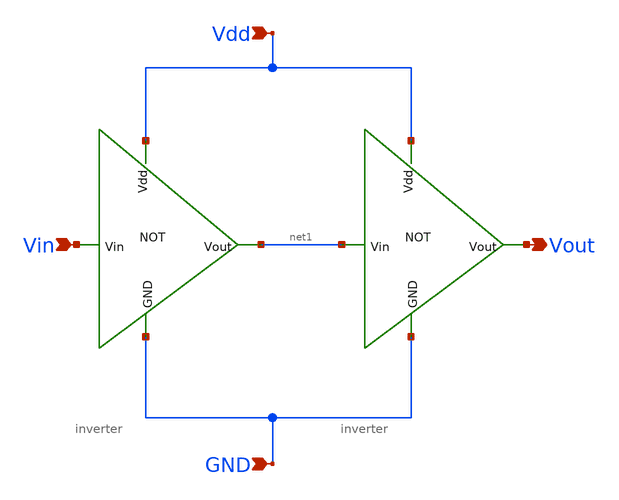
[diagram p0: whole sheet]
** sch_path: buffer.sch
**.subckt buffer Vin GND Vdd Vout
*.ipin Vin
*.ipin GND
*.ipin Vdd
*.opin Vout
x1 Vdd Vin net1 GND inverter
x2 Vdd net1 Vout GND inverter
**.ends

* expanding   symbol:  /home/jetha/Projects/sky130/SAR_ADC/inverter/inverter.sym # of pins=4
** sym_path: inverter.sym
** sch_path: inverter.sch
.subckt inverter Vdd Vin Vout GND
*.ipin Vin
*.ipin Vdd
*.ipin GND
*.opin Vout
XM2 Vout Vin GND GND sky130_fd_pr__nfet_01v8 L=0.15 W=1 nf=1 ad='int((1 + 1)/2) * 1 / 1 * 0.29' as='int((1 + 2)/2) * 1 / 1 * 0.29'
+ pd='2*int((1 + 1)/2) * (1 / 1 + 0.29)' ps='2*int((1 + 2)/2) * (1 / 1 + 0.29)' nrd='0.29 / 1 ' nrs='0.29 / 1 '
+ sa=0 sb=0 sd=0 mult=1 m=1
XM1 Vout Vin Vdd Vdd sky130_fd_pr__pfet_01v8 L=0.15 W=2 nf=1 ad='int((1 + 1)/2) * 2 / 1 * 0.29' as='int((1 + 2)/2) * 2 / 1 * 0.29'
+ pd='2*int((1 + 1)/2) * (2 / 1 + 0.29)' ps='2*int((1 + 2)/2) * (2 / 1 + 0.29)' nrd='0.29 / 2 ' nrs='0.29 / 2 '
+ sa=0 sb=0 sd=0 mult=1 m=1
.ends

.end
